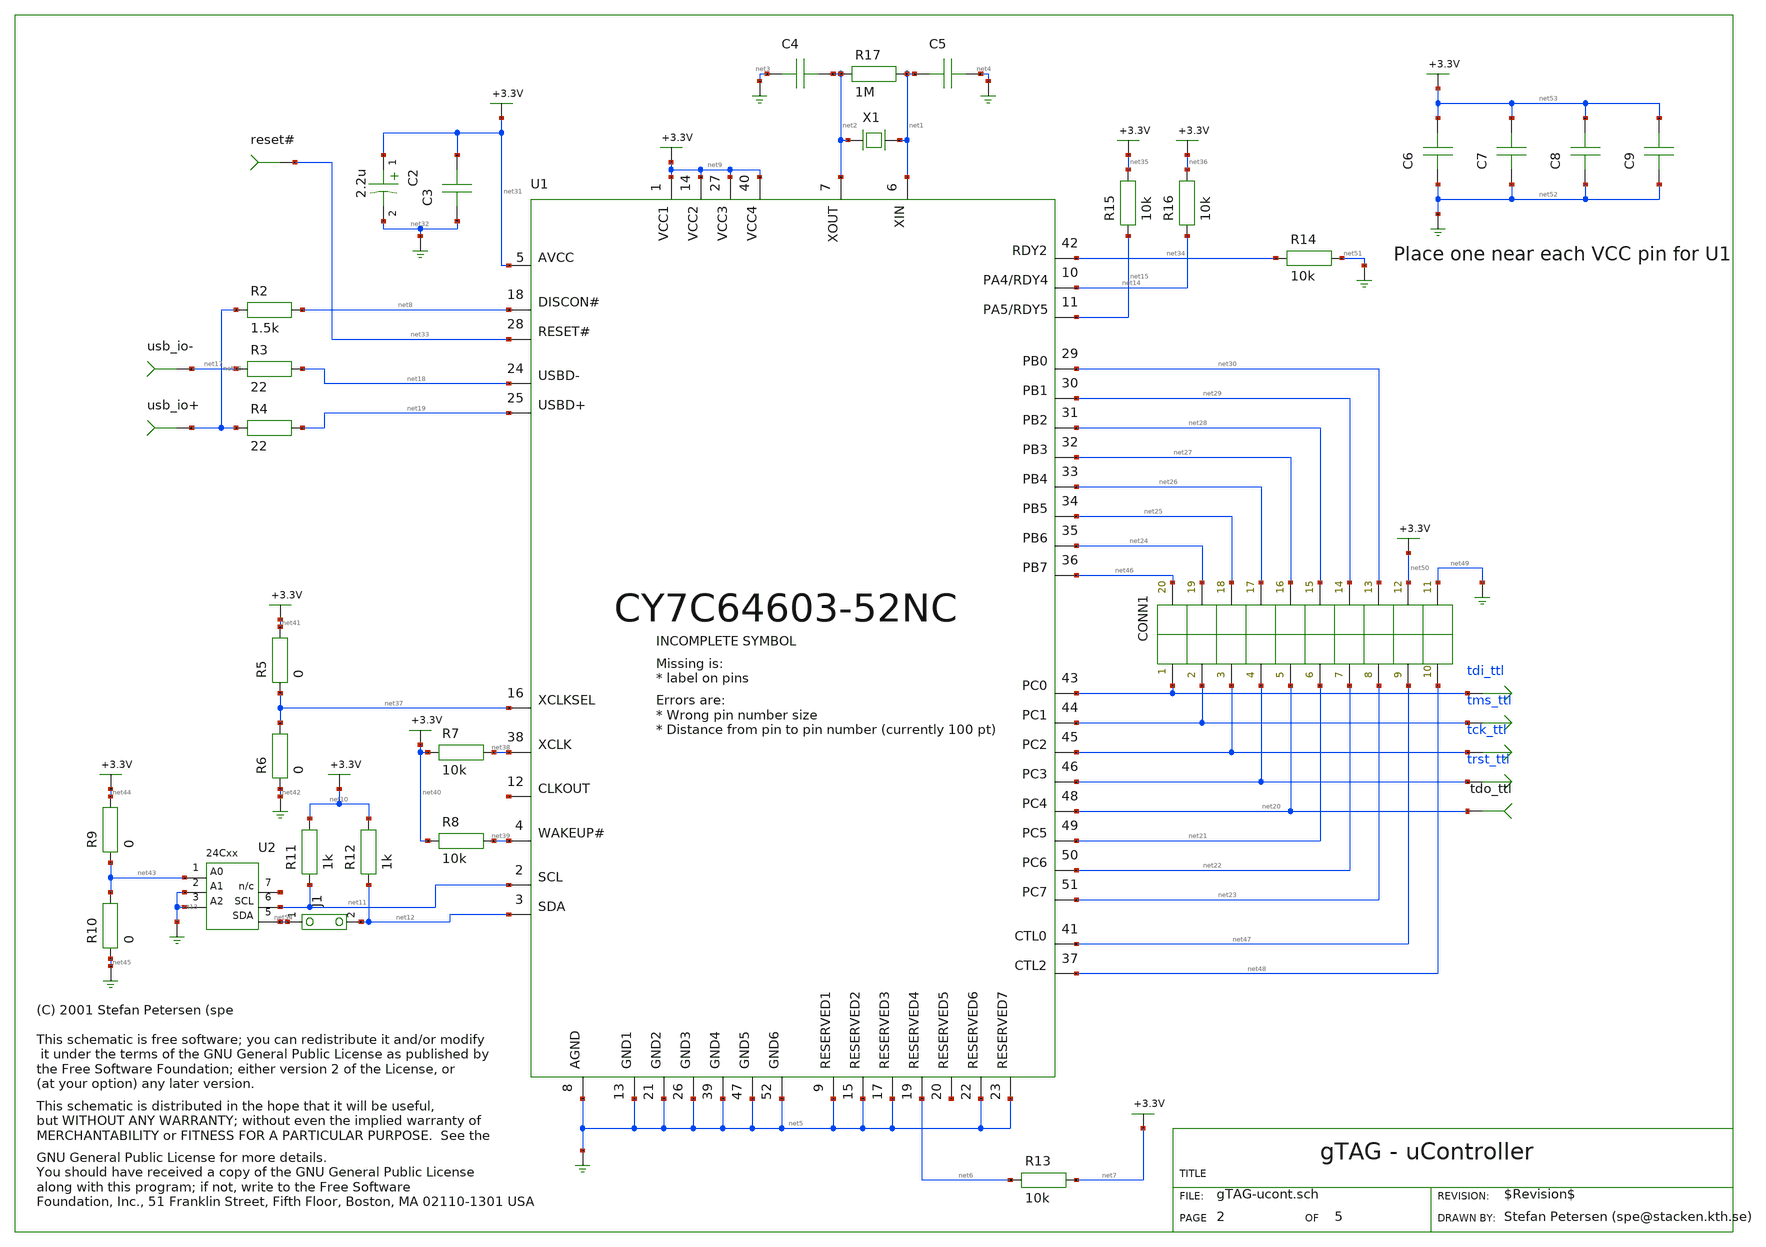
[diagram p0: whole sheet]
** sch_path: xschem_library/gschem_import/gTAG-ucont.sch
* copyleft.sym
**.subckt gTAG-ucont
U2 net54 net43 net13 net11 net13 net55
X1 net2 net1 12MHz
R17 net2 net1 1M
C4 net3 net2 30p
C5 net1 net4 30p
R13 net6 net7 10k
usb_io+ net16
usb_io- net17
R2 net16 net8 1.5k
R12 net12 net10 1k
R11 net11 net10 1k
R6 net42 net37 0
R15 net15 net35 10k
R4 net16 net19 22
R3 net17 net18 22
R5 net37 net41 0
R7 net40 net38 10k
R8 net40 net39 10k
C3 net32 net31 100n
C2 net31 net32 2.2u
U1 net31 net8 net18 net33 net19 net37 net38 net11 net56 net39 net12 net30 net29 net28 net27 net26
+ net25 net24 net46 xxx xxx xxx xxx net20 net21 net22 net23 net34 net14 net15 net47 net48 net5 net5 net57
+ net6 net5 net5 net5 net5 net5 net5 net5 net5 net5 net5 net9 net9 net9 net2 net1 net9
tdo_ttl net20
R16 net14 net36 10k
R14 net34 net51 10k
R10 net45 net43 0
R9 net43 net44 0
C6 net52 net53 100n
C7 net52 net53 100n
C8 net52 net53 100n
C9 net52 net53 100n
J1 net12 net54
reset# net33
CONN1 xxx xxx xxx xxx net20 net21 net22 net23 net47 net48 net49 net50 net30 net29 net28 net27 net26
+ net25 net24 net46
**.ends
.end
